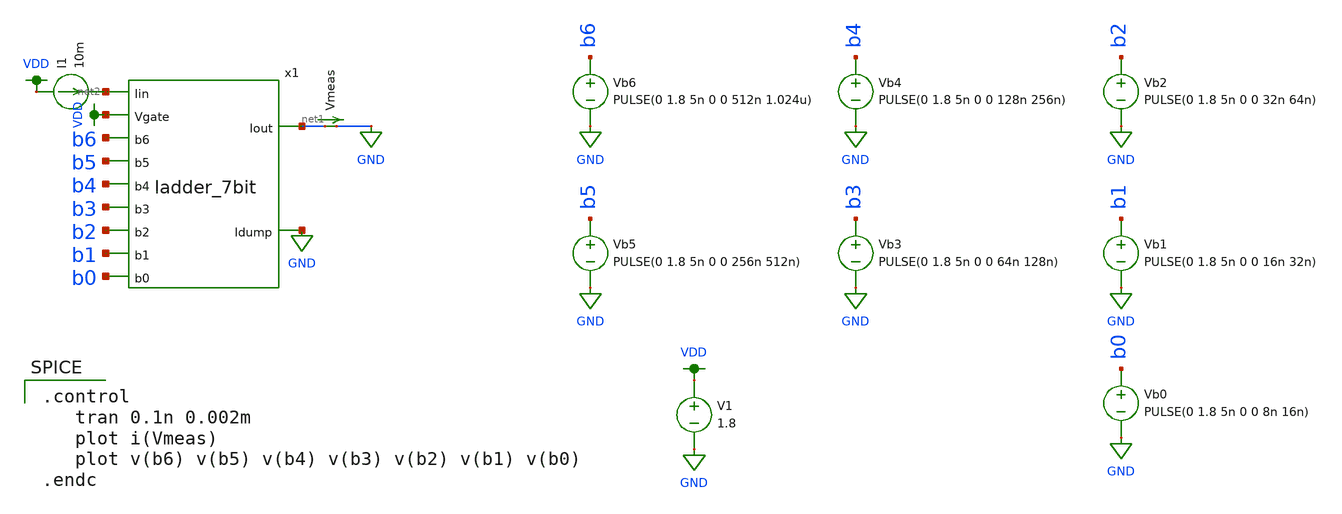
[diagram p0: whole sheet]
** sch_path: dac_test.sch
**.subckt dac_test
x1 VDD net2 GND net1 b5 b4 b1 b2 b3 b0 b6 ladder_7bit
I1 VDD net2 10m
Vmeas net1 GND 0
.save i(vmeas)
Vb0 b0 GND PULSE(0 1.8 5n 0 0 8n 16n)
Vb1 b1 GND PULSE(0 1.8 5n 0 0 16n 32n)
Vb2 b2 GND PULSE(0 1.8 5n 0 0 32n 64n)
Vb3 b3 GND PULSE(0 1.8 5n 0 0 64n 128n)
Vb4 b4 GND PULSE(0 1.8 5n 0 0 128n 256n)
Vb5 b5 GND PULSE(0 1.8 5n 0 0 256n 512n)
Vb6 b6 GND PULSE(0 1.8 5n 0 0 512n 1.024u)
V1 VDD GND 1.8
**** begin user architecture code

.option wnflag=1
.param MC_SWITCH=0.0
.lib ~/skywater/skywater-pdk/libraries/sky130_fd_pr_ngspice/latest/models/sky130.lib.spice tt


.control
   tran 0.1n 0.002m
   plot i(Vmeas)
   plot v(b6) v(b5) v(b4) v(b3) v(b2) v(b1) v(b0)
.endc

**** end user architecture code
**.ends

* expanding   symbol:  /home/madvlsi/R2R-DAC/ladder_7bit.sym # of pins=11
** sym_path: ladder_7bit.sym
** sch_path: ladder_7bit.sch
.subckt ladder_7bit Vgate Iin Idump Iout b5 b4 b1 b2 b3 b0 b6
*.opin Idump
*.opin Iout
*.ipin Vgate
*.ipin Iin
*.ipin b6
*.ipin b5
*.ipin b4
*.ipin b3
*.ipin b2
*.ipin b1
*.ipin b0
x1 Iin net8 Vgate Idump Iout net1 b6 ladder_1bit
x2 net8 net9 Vgate Idump Iout net2 b5 ladder_1bit
x3 net9 net10 Vgate Idump Iout net3 b4 ladder_1bit
x4 net10 net11 Vgate Idump Iout net4 b3 ladder_1bit
x5 net11 net12 Vgate Idump Iout net5 b2 ladder_1bit
x6 net12 net13 Vgate Idump Iout net6 b1 ladder_1bit
x7 net13 net14 Vgate Idump Iout net7 b0 ladder_1bit
XM1 Idump Vgate net14 GND sky130_fd_pr__nfet_01v8 L=0.15 W=1 nf=1 ad='int((nf+1)/2) * W/nf * 0.29' as='int((nf+2)/2) * W/nf * 0.29'
+ pd='2*int((nf+1)/2) * (W/nf + 0.29)' ps='2*int((nf+2)/2) * (W/nf + 0.29)' nrd='0.29 / W' nrs='0.29 / W'
+ sa=0 sb=0 sd=0 mult=1 m=1
X8 b6 net15 VDD GND inverter
X9 b5 net16 VDD GND inverter
X10 b4 net17 VDD GND inverter
X11 b3 net18 VDD GND inverter
X12 b2 net19 VDD GND inverter
X13 b1 net20 VDD GND inverter
X14 b0 net21 VDD GND inverter
.ends


* expanding   symbol:  /home/madvlsi/R2R-DAC/ladder_1bit.sym # of pins=7
** sym_path: ladder_1bit.sym
** sch_path: ladder_1bit.sch
.subckt ladder_1bit Iin_in Iin_out Vg I_dump Iout B_bar B
*.ipin Iin_in
*.ipin Vg
*.ipin B
*.ipin B_bar
*.opin Iin_out
*.opin I_dump
*.opin Iout
XM5 net1 Vg Iin_in GND sky130_fd_pr__nfet_01v8 L=0.15 W=1 nf=1 ad='int((nf+1)/2) * W/nf * 0.29' as='int((nf+2)/2) * W/nf * 0.29'
+ pd='2*int((nf+1)/2) * (W/nf + 0.29)' ps='2*int((nf+2)/2) * (W/nf + 0.29)' nrd='0.29 / W' nrs='0.29 / W'
+ sa=0 sb=0 sd=0 mult=1 m=1
XM6 Iout B net1 GND sky130_fd_pr__nfet_01v8 L=0.15 W=1 nf=1 ad='int((nf+1)/2) * W/nf * 0.29' as='int((nf+2)/2) * W/nf * 0.29'
+ pd='2*int((nf+1)/2) * (W/nf + 0.29)' ps='2*int((nf+2)/2) * (W/nf + 0.29)' nrd='0.29 / W' nrs='0.29 / W'
+ sa=0 sb=0 sd=0 mult=1 m=1
XM7 net1 B_bar I_dump GND sky130_fd_pr__nfet_01v8 L=0.15 W=1 nf=1 ad='int((nf+1)/2) * W/nf * 0.29' as='int((nf+2)/2) * W/nf * 0.29'
+ pd='2*int((nf+1)/2) * (W/nf + 0.29)' ps='2*int((nf+2)/2) * (W/nf + 0.29)' nrd='0.29 / W' nrs='0.29 / W'
+ sa=0 sb=0 sd=0 mult=1 m=1
XM8 Iin_in Vg Iin_out GND sky130_fd_pr__nfet_01v8 L=0.15 W=1 nf=1 ad='int((nf+1)/2) * W/nf * 0.29' as='int((nf+2)/2) * W/nf * 0.29'
+ pd='2*int((nf+1)/2) * (W/nf + 0.29)' ps='2*int((nf+2)/2) * (W/nf + 0.29)' nrd='0.29 / W' nrs='0.29 / W'
+ sa=0 sb=0 sd=0 mult=1 m=1
.ends


* expanding   symbol:  /home/madvlsi/Documents/mp1/inverter.sym # of pins=4
** sym_path: /home/madvlsi/Documents/mp1/inverter.sym
** sch_path: /home/madvlsi/Documents/mp1/inverter.sch
.subckt inverter A Y VP VN
*.ipin A
*.iopin VP
*.iopin VN
*.opin Y
XM3 Y A VP VP sky130_fd_pr__pfet_01v8 L=0.15 W=1 nf=1 ad='int((nf+1)/2) * W/nf * 0.29' as='int((nf+2)/2) * W/nf * 0.29'
+ pd='2*int((nf+1)/2) * (W/nf + 0.29)' ps='2*int((nf+2)/2) * (W/nf + 0.29)' nrd='0.29 / W' nrs='0.29 / W'
+ sa=0 sb=0 sd=0 mult=1 m=1
XM4 Y A VN VN sky130_fd_pr__nfet_01v8 L=0.15 W=1 nf=1 ad='int((nf+1)/2) * W/nf * 0.29' as='int((nf+2)/2) * W/nf * 0.29'
+ pd='2*int((nf+1)/2) * (W/nf + 0.29)' ps='2*int((nf+2)/2) * (W/nf + 0.29)' nrd='0.29 / W' nrs='0.29 / W'
+ sa=0 sb=0 sd=0 mult=1 m=1
.ends

.GLOBAL GND
.GLOBAL VDD
.end
